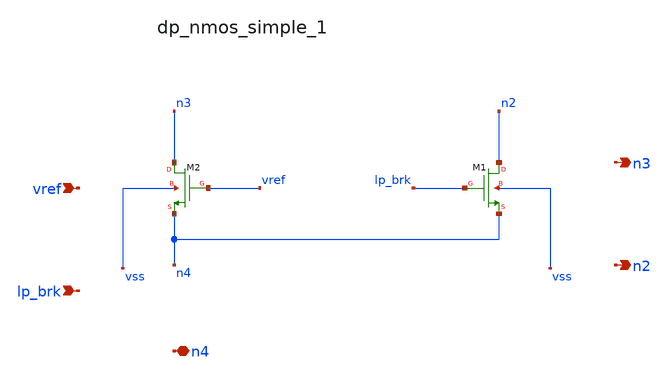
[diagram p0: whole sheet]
** sch_path: analog-db/raw/ldo_002_analoggym_folded_cascode/hier/blocks/dp_nmos_simple_1.sch
**.subckt dp_nmos_simple_1 vref lp_brk n4 n3 n2
*.ipin vref
*.ipin lp_brk
*.iopin n4
*.opin n3
*.opin n2
XM1 n2 lp_brk n4 vss sg13_hv_nmos w=x_dut_xm1_w l=x_dut_xm1_l ng=1 m=1
XM2 n3 vref n4 vss sg13_hv_nmos w=x_dut_xm2_w l=x_dut_xm2_l ng=1 m=1
**.ends
.end
